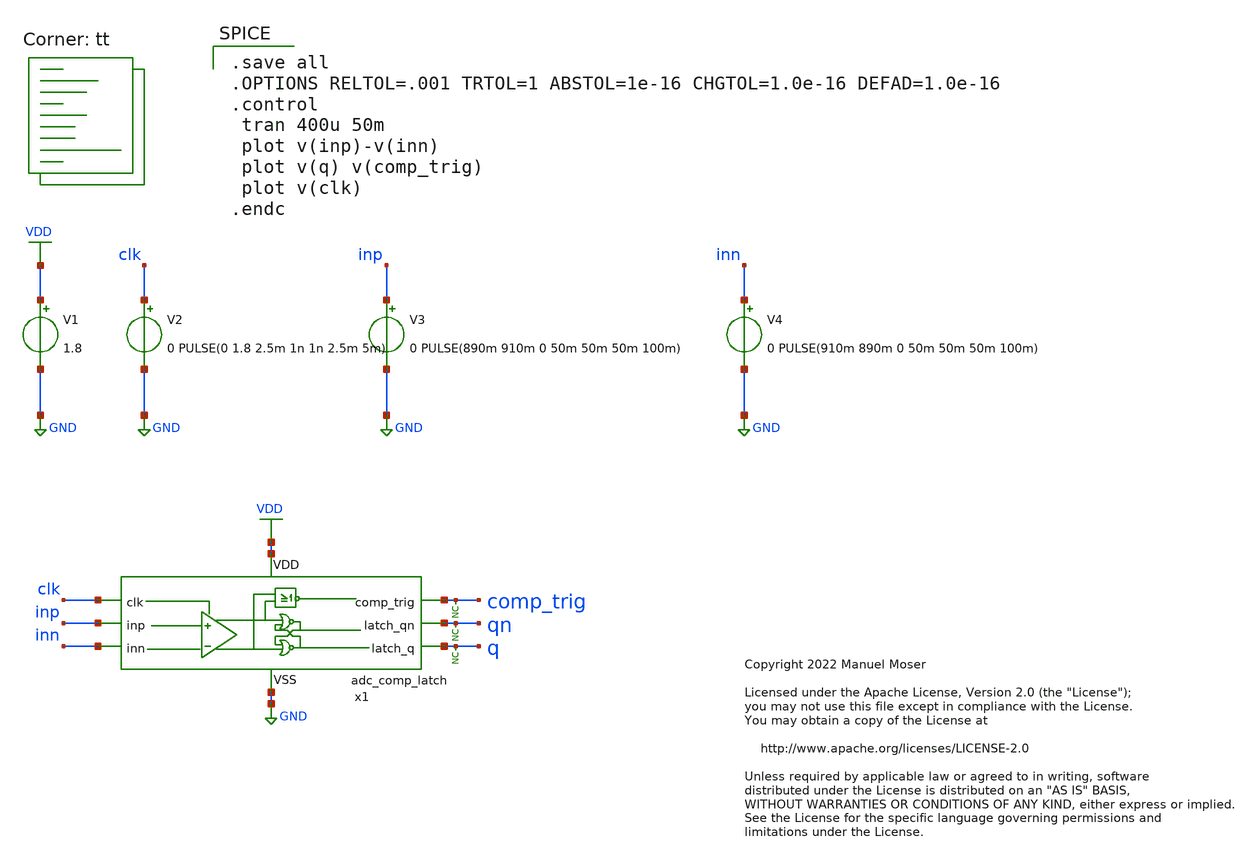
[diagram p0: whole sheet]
** sch_path: xschem/adc_comp_latch/adc_comp_latch_tb.sch
* Copyright 2022 Manuel Moser
* Licensed under the Apache License, Version 2.0 (the "License");
**.subckt adc_comp_latch_tb
V1 VDD GND 1.8
V2 clk GND 0 PULSE(0 1.8 2.5m 1n 1n 2.5m 5m)
V3 inp GND 0 PULSE(890m 910m 0 50m 50m 50m 100m)
V4 inn GND 0 PULSE(910m 890m 0 50m 50m 50m 100m)
* noconn q
x1 VDD GND comp_trig clk inp qn q inn adc_comp_latch
* noconn comp_trig
* noconn qn
**** begin user architecture code
.lib $::SKYWATER_MODELS/sky130.lib.spice tt

.save all
.OPTIONS RELTOL=.001 TRTOL=1 ABSTOL=1e-16 CHGTOL=1.0e-16 DEFAD=1.0e-16
.control
 tran 400u 50m
 plot v(inp)-v(inn)
 plot v(q) v(comp_trig)
 plot v(clk)
.endc

**** end user architecture code
**.ends
.GLOBAL GND
.GLOBAL VDD
.end
